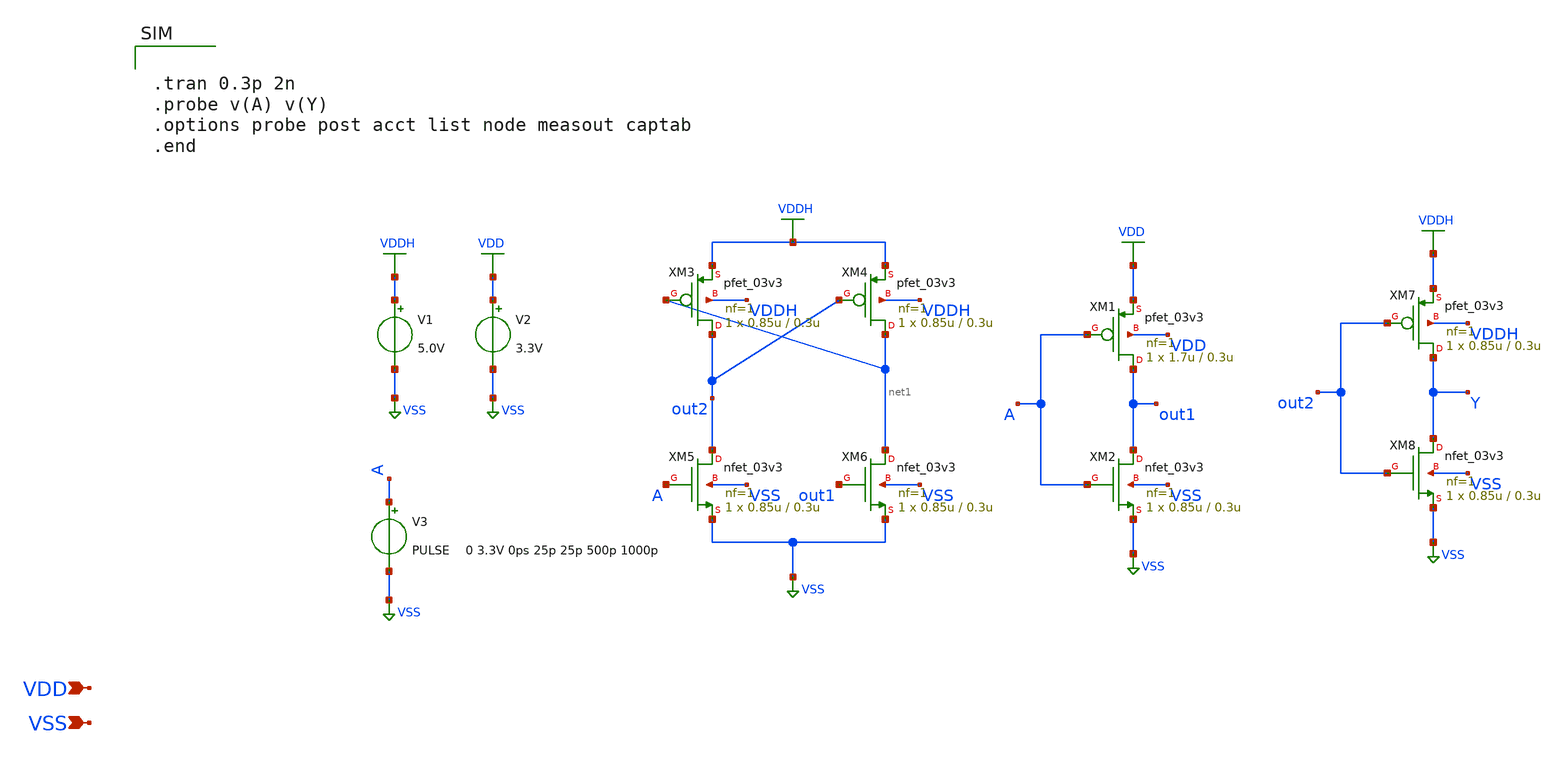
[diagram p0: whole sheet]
** sch_path: gf180mcu_osu_sc_gp9t3v3/xschem/gf180mcu_osu_sc_gp9t3v3__lshifup.sch
**.subckt gf180mcu_osu_sc_gp9t3v3__lshifup VDD VSS
*.ipin VDD
*.ipin VSS
XM1 out1 A VDD VDD pfet_03v3 L=0.3u W=1.7u nf=1 ad='int((nf+1)/2) * W/nf * 0.18u' as='int((nf+2)/2) * W/nf * 0.18u'
+ pd='2*int((nf+1)/2) * (W/nf + 0.18u)' ps='2*int((nf+2)/2) * (W/nf + 0.18u)' nrd='0.18u / W' nrs='0.18u / W'
+ sa=0 sb=0 sd=0 m=1
XM2 out1 A VSS VSS nfet_03v3 L=0.3u W=0.85u nf=1 ad='int((nf+1)/2) * W/nf * 0.18u' as='int((nf+2)/2) * W/nf * 0.18u'
+ pd='2*int((nf+1)/2) * (W/nf + 0.18u)' ps='2*int((nf+2)/2) * (W/nf + 0.18u)' nrd='0.18u / W' nrs='0.18u / W'
+ sa=0 sb=0 sd=0 m=1
XM3 out2 net1 VDDH VDDH pfet_03v3 L=0.3u W=0.85u nf=1 ad='int((nf+1)/2) * W/nf * 0.18u' as='int((nf+2)/2) * W/nf * 0.18u'
+ pd='2*int((nf+1)/2) * (W/nf + 0.18u)' ps='2*int((nf+2)/2) * (W/nf + 0.18u)' nrd='0.18u / W' nrs='0.18u / W'
+ sa=0 sb=0 sd=0 m=1
XM4 net1 out2 VDDH VDDH pfet_03v3 L=0.3u W=0.85u nf=1 ad='int((nf+1)/2) * W/nf * 0.18u' as='int((nf+2)/2) * W/nf * 0.18u'
+ pd='2*int((nf+1)/2) * (W/nf + 0.18u)' ps='2*int((nf+2)/2) * (W/nf + 0.18u)' nrd='0.18u / W' nrs='0.18u / W'
+ sa=0 sb=0 sd=0 m=1
XM5 out2 A VSS VSS nfet_03v3 L=0.3u W=0.85u nf=1 ad='int((nf+1)/2) * W/nf * 0.18u' as='int((nf+2)/2) * W/nf * 0.18u'
+ pd='2*int((nf+1)/2) * (W/nf + 0.18u)' ps='2*int((nf+2)/2) * (W/nf + 0.18u)' nrd='0.18u / W' nrs='0.18u / W'
+ sa=0 sb=0 sd=0 m=1
XM6 net1 out1 VSS VSS nfet_03v3 L=0.3u W=0.85u nf=1 ad='int((nf+1)/2) * W/nf * 0.18u' as='int((nf+2)/2) * W/nf * 0.18u'
+ pd='2*int((nf+1)/2) * (W/nf + 0.18u)' ps='2*int((nf+2)/2) * (W/nf + 0.18u)' nrd='0.18u / W' nrs='0.18u / W'
+ sa=0 sb=0 sd=0 m=1
XM7 Y out2 VDDH VDDH pfet_03v3 L=0.3u W=0.85u nf=1 ad='int((nf+1)/2) * W/nf * 0.18u' as='int((nf+2)/2) * W/nf * 0.18u'
+ pd='2*int((nf+1)/2) * (W/nf + 0.18u)' ps='2*int((nf+2)/2) * (W/nf + 0.18u)' nrd='0.18u / W' nrs='0.18u / W'
+ sa=0 sb=0 sd=0 m=1
XM8 Y out2 VSS VSS nfet_03v3 L=0.3u W=0.85u nf=1 ad='int((nf+1)/2) * W/nf * 0.18u' as='int((nf+2)/2) * W/nf * 0.18u'
+ pd='2*int((nf+1)/2) * (W/nf + 0.18u)' ps='2*int((nf+2)/2) * (W/nf + 0.18u)' nrd='0.18u / W' nrs='0.18u / W'
+ sa=0 sb=0 sd=0 m=1
V1 VDDH VSS 5.0V
V2 VDD VSS 3.3V
V3 A VSS PULSE 0 3.3V 0ps 25p 25p 500p 1000p
**** begin user architecture code

.temp 25
.inc "/import/yukari1/lrburle/OSU_180/char/techfiles/design.hspice"
.lib "/import/yukari1/lrburle/OSU_180/char/techfiles/sm141064.hspice" typical



.tran 0.3p 2n
.probe v(A) v(Y)
.options probe post acct list node measout captab
.end


**** end user architecture code
**.ends
.GLOBAL VDD
.GLOBAL VSS
.GLOBAL VDDH
.end
